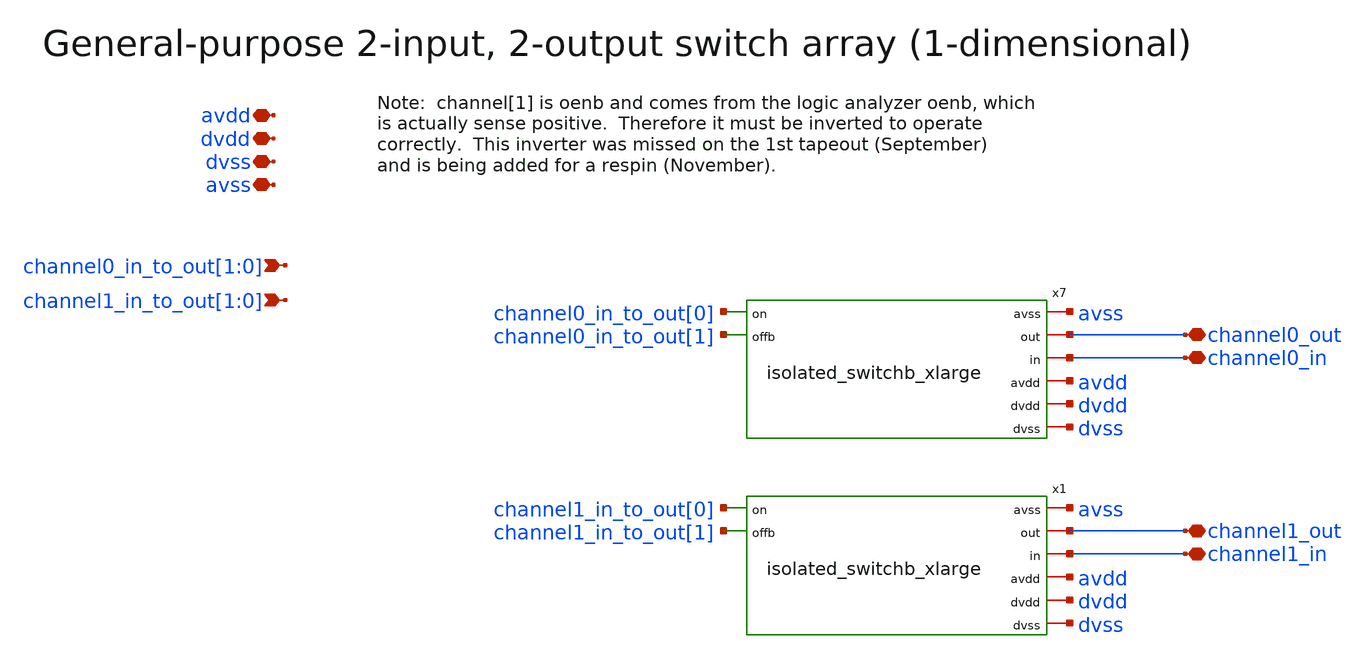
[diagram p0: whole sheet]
** sch_path: xschem/switch_array_2.sch
**.subckt switch_array_2 channel0_in avdd dvdd dvss avss channel0_in_to_out[1],channel0_in_to_out[0]
*+ channel0_out channel1_in channel1_out channel1_in_to_out[1],channel1_in_to_out[0]
*.iopin channel0_in
*.iopin avdd
*.iopin dvdd
*.iopin dvss
*.iopin avss
*.ipin channel0_in_to_out[1],channel0_in_to_out[0]
*.iopin channel0_out
*.iopin channel1_in
*.iopin channel1_out
*.ipin channel1_in_to_out[1],channel1_in_to_out[0]
x7 avss channel0_in_to_out[0] channel0_out channel0_in avdd dvdd dvss channel0_in_to_out[1]
+ isolated_switchb_xlarge
x1 avss channel1_in_to_out[0] channel1_out channel1_in avdd dvdd dvss channel1_in_to_out[1]
+ isolated_switchb_xlarge
**.ends
.end
